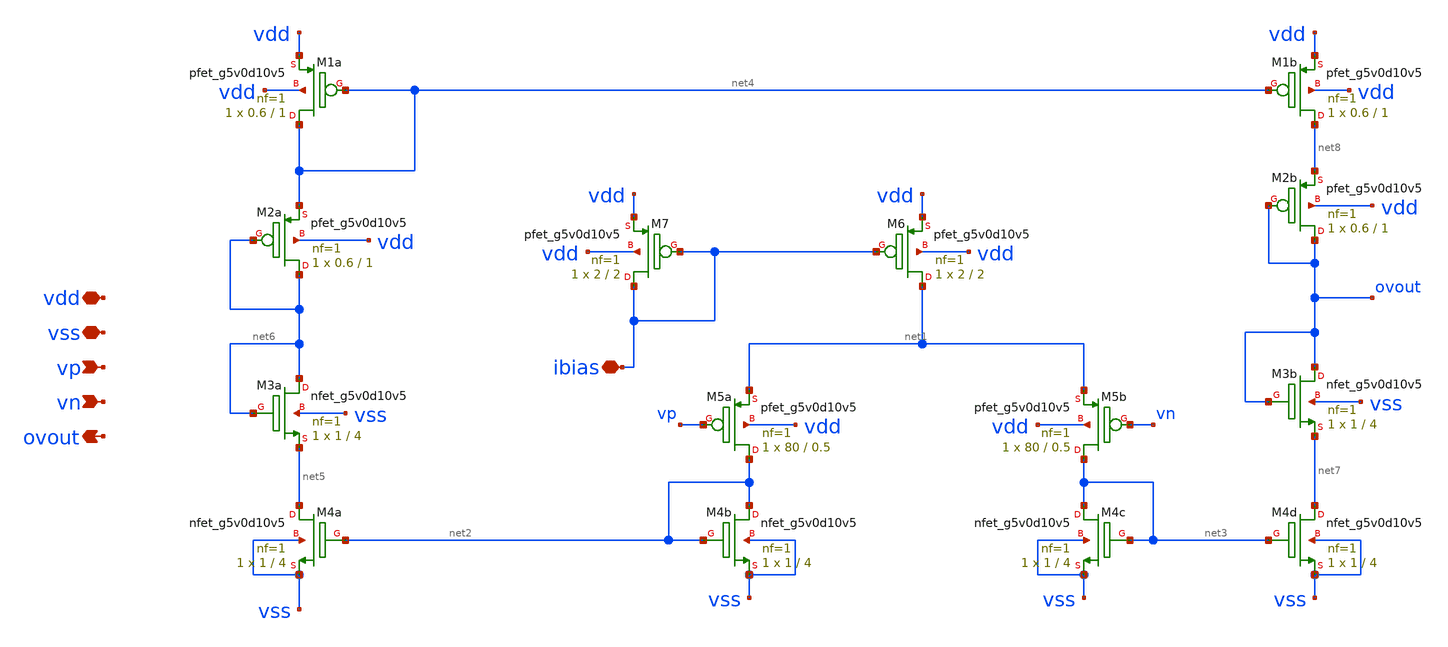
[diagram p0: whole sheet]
** sch_path: xschem/OTA.sch
**.subckt OTA ibias vdd vss vp vn ovout
*.iopin ibias
*.iopin vdd
*.iopin vss
*.ipin vp
*.ipin vn
*.opin ovout
XM5a net2 vp net1 vdd sky130_fd_pr__pfet_g5v0d10v5 L=0.5 W=80 nf=1 ad='int((nf+1)/2) * W/nf * 0.29' as='int((nf+2)/2) * W/nf * 0.29'
+ pd='2*int((nf+1)/2) * (W/nf + 0.29)' ps='2*int((nf+2)/2) * (W/nf + 0.29)' nrd='0.29 / W' nrs='0.29 / W'
+ sa=0 sb=0 sd=0 mult=1 m=1
XM5b net3 vn net1 vdd sky130_fd_pr__pfet_g5v0d10v5 L=0.5 W=80 nf=1 ad='int((nf+1)/2) * W/nf * 0.29' as='int((nf+2)/2) * W/nf * 0.29'
+ pd='2*int((nf+1)/2) * (W/nf + 0.29)' ps='2*int((nf+2)/2) * (W/nf + 0.29)' nrd='0.29 / W' nrs='0.29 / W'
+ sa=0 sb=0 sd=0 mult=1 m=1
XM4b net2 net2 vss vss sky130_fd_pr__nfet_g5v0d10v5 L=4 W=1 nf=1 ad='int((nf+1)/2) * W/nf * 0.29' as='int((nf+2)/2) * W/nf * 0.29'
+ pd='2*int((nf+1)/2) * (W/nf + 0.29)' ps='2*int((nf+2)/2) * (W/nf + 0.29)' nrd='0.29 / W' nrs='0.29 / W'
+ sa=0 sb=0 sd=0 mult=1 m=1
XM4c net3 net3 vss vss sky130_fd_pr__nfet_g5v0d10v5 L=4 W=1 nf=1 ad='int((nf+1)/2) * W/nf * 0.29' as='int((nf+2)/2) * W/nf * 0.29'
+ pd='2*int((nf+1)/2) * (W/nf + 0.29)' ps='2*int((nf+2)/2) * (W/nf + 0.29)' nrd='0.29 / W' nrs='0.29 / W'
+ sa=0 sb=0 sd=0 mult=1 m=1
XM4a net5 net2 vss vss sky130_fd_pr__nfet_g5v0d10v5 L=4 W=1 nf=1 ad='int((nf+1)/2) * W/nf * 0.29' as='int((nf+2)/2) * W/nf * 0.29'
+ pd='2*int((nf+1)/2) * (W/nf + 0.29)' ps='2*int((nf+2)/2) * (W/nf + 0.29)' nrd='0.29 / W' nrs='0.29 / W'
+ sa=0 sb=0 sd=0 mult=1 m=1
XM4d net7 net3 vss vss sky130_fd_pr__nfet_g5v0d10v5 L=4 W=1 nf=1 ad='int((nf+1)/2) * W/nf * 0.29' as='int((nf+2)/2) * W/nf * 0.29'
+ pd='2*int((nf+1)/2) * (W/nf + 0.29)' ps='2*int((nf+2)/2) * (W/nf + 0.29)' nrd='0.29 / W' nrs='0.29 / W'
+ sa=0 sb=0 sd=0 mult=1 m=1
XM1a net4 net4 vdd vdd sky130_fd_pr__pfet_g5v0d10v5 L=1 W=0.6 nf=1 ad='int((nf+1)/2) * W/nf * 0.29' as='int((nf+2)/2) * W/nf * 0.29'
+ pd='2*int((nf+1)/2) * (W/nf + 0.29)' ps='2*int((nf+2)/2) * (W/nf + 0.29)' nrd='0.29 / W' nrs='0.29 / W'
+ sa=0 sb=0 sd=0 mult=1 m=1
XM1b net8 net4 vdd vdd sky130_fd_pr__pfet_g5v0d10v5 L=1 W=0.6 nf=1 ad='int((nf+1)/2) * W/nf * 0.29' as='int((nf+2)/2) * W/nf * 0.29'
+ pd='2*int((nf+1)/2) * (W/nf + 0.29)' ps='2*int((nf+2)/2) * (W/nf + 0.29)' nrd='0.29 / W' nrs='0.29 / W'
+ sa=0 sb=0 sd=0 mult=1 m=1
XM7 ibias ibias vdd vdd sky130_fd_pr__pfet_g5v0d10v5 L=2 W=2 nf=1 ad='int((nf+1)/2) * W/nf * 0.29' as='int((nf+2)/2) * W/nf * 0.29'
+ pd='2*int((nf+1)/2) * (W/nf + 0.29)' ps='2*int((nf+2)/2) * (W/nf + 0.29)' nrd='0.29 / W' nrs='0.29 / W'
+ sa=0 sb=0 sd=0 mult=1 m=1
XM6 net1 ibias vdd vdd sky130_fd_pr__pfet_g5v0d10v5 L=2 W=2 nf=1 ad='int((nf+1)/2) * W/nf * 0.29' as='int((nf+2)/2) * W/nf * 0.29'
+ pd='2*int((nf+1)/2) * (W/nf + 0.29)' ps='2*int((nf+2)/2) * (W/nf + 0.29)' nrd='0.29 / W' nrs='0.29 / W'
+ sa=0 sb=0 sd=0 mult=1 m=1
XM3a net6 net6 net5 vss sky130_fd_pr__nfet_g5v0d10v5 L=4 W=1 nf=1 ad='int((nf+1)/2) * W/nf * 0.29' as='int((nf+2)/2) * W/nf * 0.29'
+ pd='2*int((nf+1)/2) * (W/nf + 0.29)' ps='2*int((nf+2)/2) * (W/nf + 0.29)' nrd='0.29 / W' nrs='0.29 / W'
+ sa=0 sb=0 sd=0 mult=1 m=1
XM2a net6 net6 net4 vdd sky130_fd_pr__pfet_g5v0d10v5 L=1 W=0.6 nf=1 ad='int((nf+1)/2) * W/nf * 0.29'
+ as='int((nf+2)/2) * W/nf * 0.29' pd='2*int((nf+1)/2) * (W/nf + 0.29)' ps='2*int((nf+2)/2) * (W/nf + 0.29)'
+ nrd='0.29 / W' nrs='0.29 / W' sa=0 sb=0 sd=0 mult=1 m=1
XM2b ovout ovout net8 vdd sky130_fd_pr__pfet_g5v0d10v5 L=1 W=0.6 nf=1 ad='int((nf+1)/2) * W/nf * 0.29'
+ as='int((nf+2)/2) * W/nf * 0.29' pd='2*int((nf+1)/2) * (W/nf + 0.29)' ps='2*int((nf+2)/2) * (W/nf + 0.29)'
+ nrd='0.29 / W' nrs='0.29 / W' sa=0 sb=0 sd=0 mult=1 m=1
XM3b ovout ovout net7 vss sky130_fd_pr__nfet_g5v0d10v5 L=4 W=1 nf=1 ad='int((nf+1)/2) * W/nf * 0.29'
+ as='int((nf+2)/2) * W/nf * 0.29' pd='2*int((nf+1)/2) * (W/nf + 0.29)' ps='2*int((nf+2)/2) * (W/nf + 0.29)'
+ nrd='0.29 / W' nrs='0.29 / W' sa=0 sb=0 sd=0 mult=1 m=1
**.ends
.end
